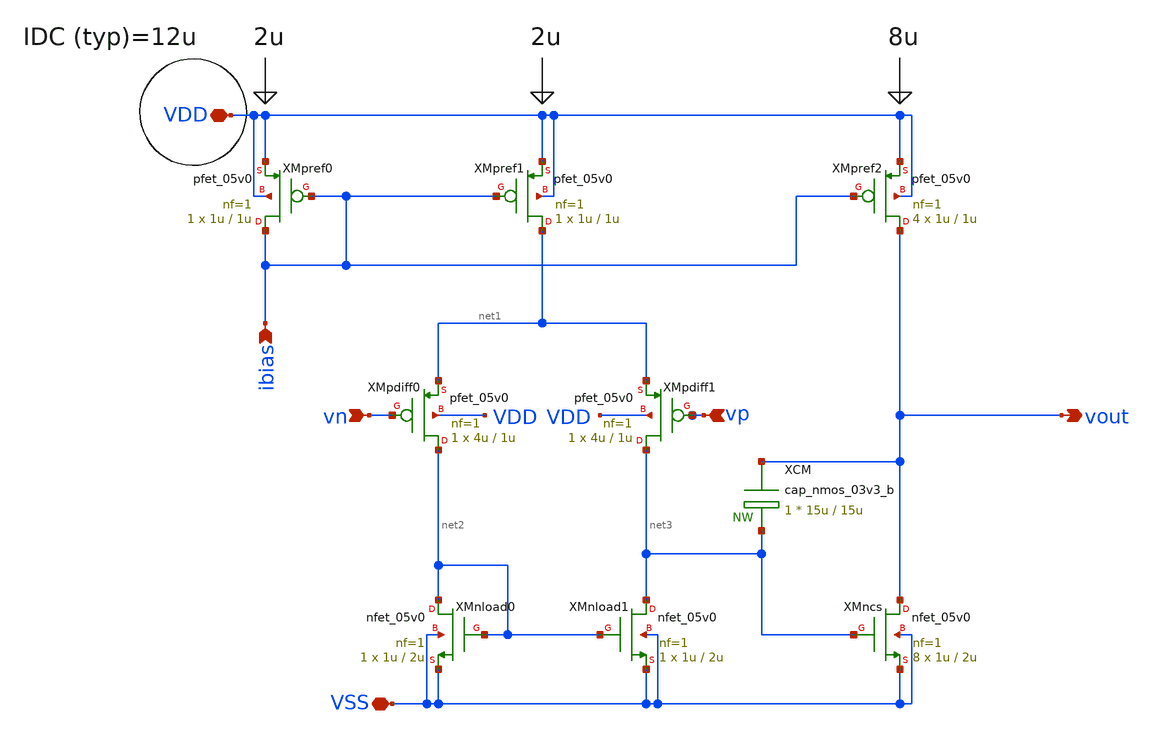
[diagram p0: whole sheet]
** sch_path: designs/libs/core_bandgap/bandgap_opamp/bandgap_opamp.sch
**.subckt bandgap_opamp vn vp vout ibias VDD VSS
*.ipin vn
*.ipin vp
*.opin vout
*.ipin ibias
*.iopin VDD
*.iopin VSS
XCM vout net3 cap_nmos_03v3_b c_width=15u c_length=15u m=1
XMpref0 ibias ibias VDD VDD pfet_05v0 L=1u W=1u nf=1 ad='int((nf+1)/2) * W/nf * 0.18u' as='int((nf+2)/2) * W/nf * 0.18u'
+ pd='2*int((nf+1)/2) * (W/nf + 0.18u)' ps='2*int((nf+2)/2) * (W/nf + 0.18u)' nrd='0.18u / W' nrs='0.18u / W'
+ sa=0 sb=0 sd=0 m=1
XMnload0 net2 net2 VSS VSS nfet_05v0 L=2u W=1u nf=1 ad='int((nf+1)/2) * W/nf * 0.18u' as='int((nf+2)/2) * W/nf * 0.18u'
+ pd='2*int((nf+1)/2) * (W/nf + 0.18u)' ps='2*int((nf+2)/2) * (W/nf + 0.18u)' nrd='0.18u / W' nrs='0.18u / W'
+ sa=0 sb=0 sd=0 m=1
XMpref1 net1 ibias VDD VDD pfet_05v0 L=1u W=1u nf=1 ad='int((nf+1)/2) * W/nf * 0.18u' as='int((nf+2)/2) * W/nf * 0.18u'
+ pd='2*int((nf+1)/2) * (W/nf + 0.18u)' ps='2*int((nf+2)/2) * (W/nf + 0.18u)' nrd='0.18u / W' nrs='0.18u / W'
+ sa=0 sb=0 sd=0 m=1
XMpref2 vout ibias VDD VDD pfet_05v0 L=1u W=1u nf=1 ad='int((nf+1)/2) * W/nf * 0.18u' as='int((nf+2)/2) * W/nf * 0.18u'
+ pd='2*int((nf+1)/2) * (W/nf + 0.18u)' ps='2*int((nf+2)/2) * (W/nf + 0.18u)' nrd='0.18u / W' nrs='0.18u / W'
+ sa=0 sb=0 sd=0 m=4
XMpdiff0 net2 vn net1 VDD pfet_05v0 L=1u W=4u nf=1 ad='int((nf+1)/2) * W/nf * 0.18u' as='int((nf+2)/2) * W/nf * 0.18u'
+ pd='2*int((nf+1)/2) * (W/nf + 0.18u)' ps='2*int((nf+2)/2) * (W/nf + 0.18u)' nrd='0.18u / W' nrs='0.18u / W'
+ sa=0 sb=0 sd=0 m=1
XMpdiff1 net3 vp net1 VDD pfet_05v0 L=1u W=4u nf=1 ad='int((nf+1)/2) * W/nf * 0.18u' as='int((nf+2)/2) * W/nf * 0.18u'
+ pd='2*int((nf+1)/2) * (W/nf + 0.18u)' ps='2*int((nf+2)/2) * (W/nf + 0.18u)' nrd='0.18u / W' nrs='0.18u / W'
+ sa=0 sb=0 sd=0 m=1
XMnload1 net3 net2 VSS VSS nfet_05v0 L=2u W=1u nf=1 ad='int((nf+1)/2) * W/nf * 0.18u' as='int((nf+2)/2) * W/nf * 0.18u'
+ pd='2*int((nf+1)/2) * (W/nf + 0.18u)' ps='2*int((nf+2)/2) * (W/nf + 0.18u)' nrd='0.18u / W' nrs='0.18u / W'
+ sa=0 sb=0 sd=0 m=1
XMncs vout net3 VSS VSS nfet_05v0 L=2u W=1u nf=1 ad='int((nf+1)/2) * W/nf * 0.18u' as='int((nf+2)/2) * W/nf * 0.18u'
+ pd='2*int((nf+1)/2) * (W/nf + 0.18u)' ps='2*int((nf+2)/2) * (W/nf + 0.18u)' nrd='0.18u / W' nrs='0.18u / W'
+ sa=0 sb=0 sd=0 m=8
**.ends
.end
